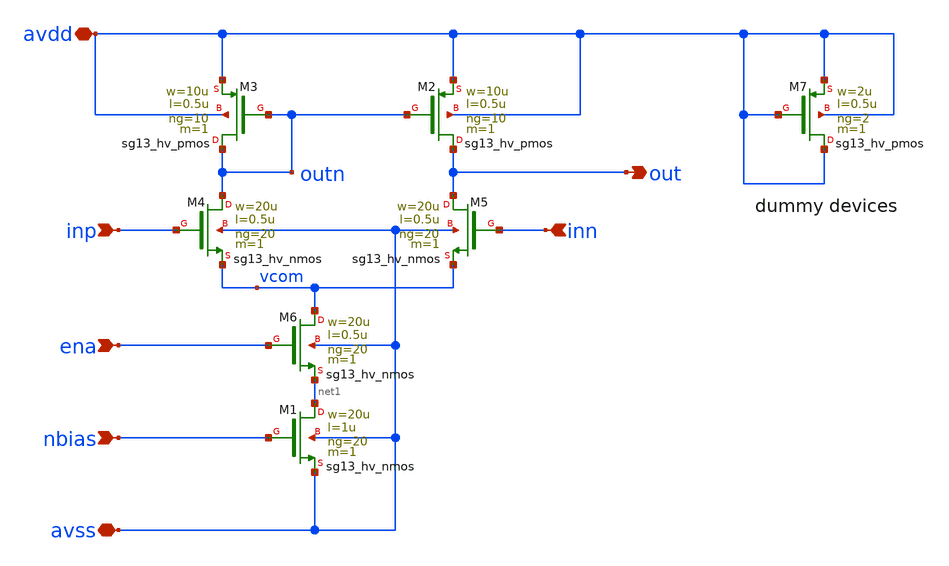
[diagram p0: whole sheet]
** sch_path: xschem/bias_amp_large.sch
**.subckt bias_amp_large inp nbias inn out avdd avss ena
*.ipin inp
*.ipin nbias
*.ipin inn
*.opin out
*.iopin avdd
*.iopin avss
*.ipin ena
XM1 net1 nbias avss avss sg13_hv_nmos w=20u l=1u ng=20 m=1 mm_ok=1
XM2 out outn avdd avdd sg13_hv_pmos w=10u l=0.5u ng=10 m=1 mm_ok=1
XM3 outn outn avdd avdd sg13_hv_pmos w=10u l=0.5u ng=10 m=1 mm_ok=1
XM4 outn inp vcom avss sg13_hv_nmos w=20u l=0.5u ng=20 m=1 mm_ok=1
XM5 out inn vcom avss sg13_hv_nmos w=20u l=0.5u ng=20 m=1 mm_ok=1
XM6 vcom ena net1 avss sg13_hv_nmos w=20u l=0.5u ng=20 m=1 mm_ok=1
XM7 avdd avdd avdd avdd sg13_hv_pmos w=2u l=0.5u ng=2 m=1 mm_ok=1
**.ends
.end
